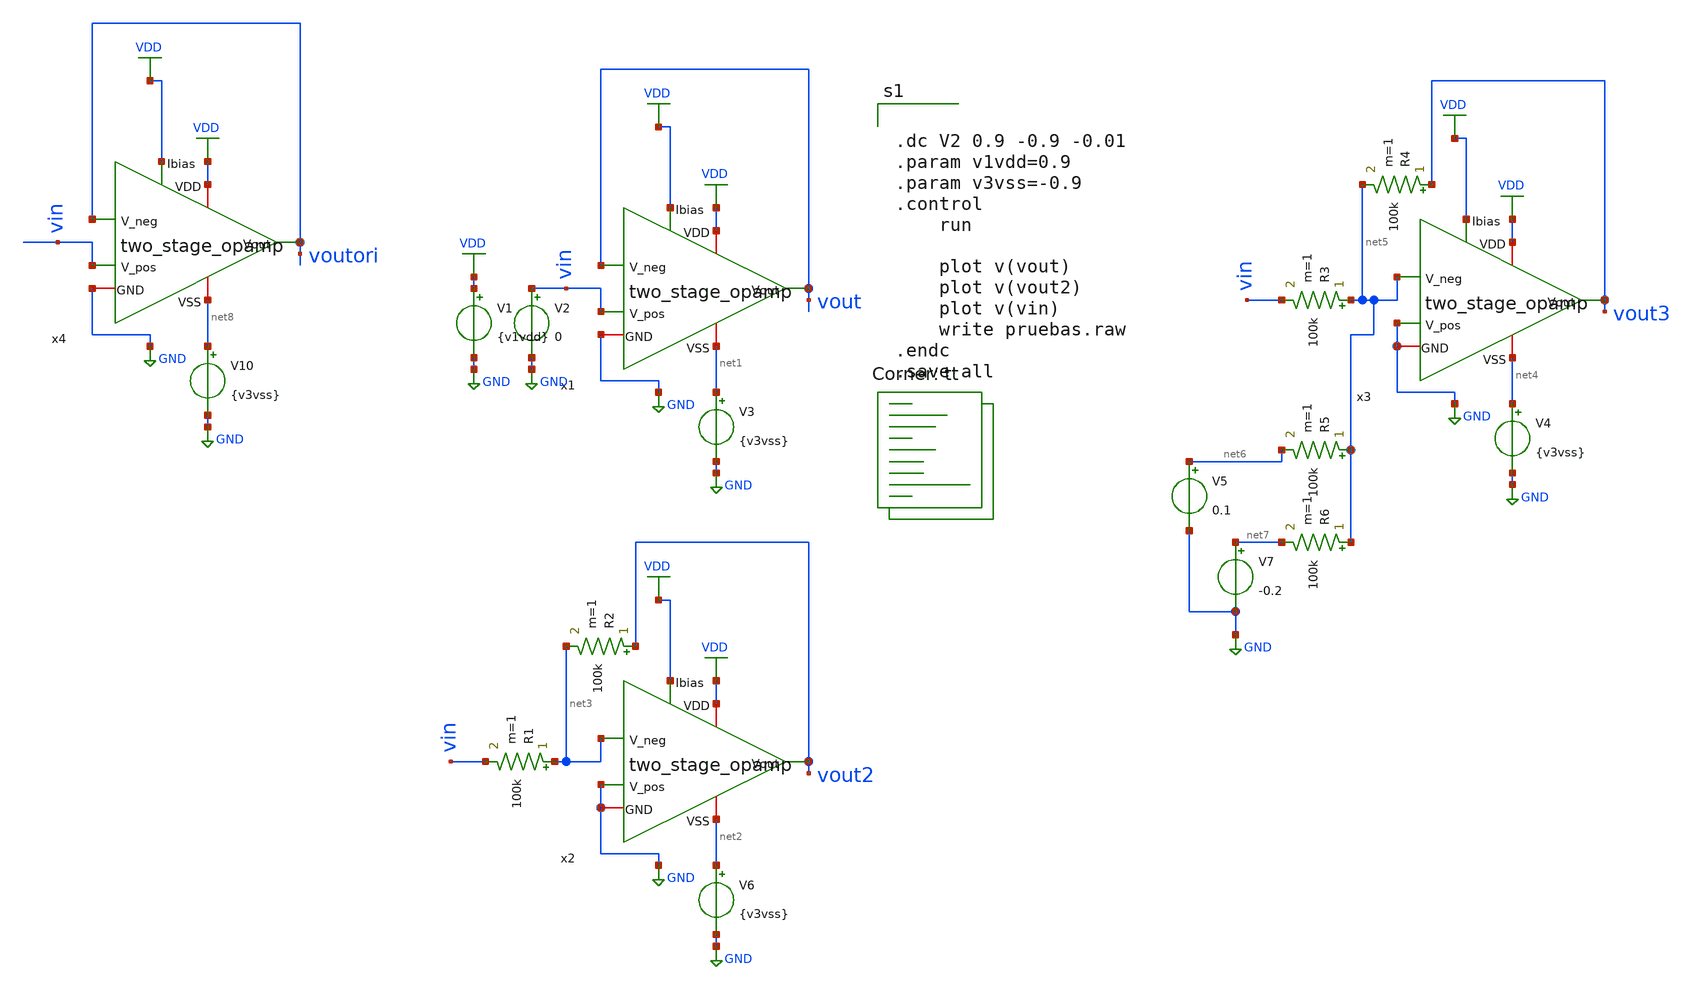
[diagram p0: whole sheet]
** sch_path: two_stage_opamp/pruebas.sch
**.subckt pruebas
x1 VDD vout VDD vout GND vin net1 two_stage_opamp W1=2.13 W2=9 W3=8.7 W4=9 W5=9.8 W6=8.7 L1=0.3965
+ L2=0.3965 L3=0.3965 L4=0.9 L5=1.2 L6=0.8
V1 VDD GND {v1vdd}
V2 vin GND 0
V3 net1 GND {v3vss}
x2 VDD vout2 VDD net3 GND GND net2 two_stage_opamp W1=2.13 W2=9 W3=8.7 W4=9 W5=9.8 W6=8.7 L1=0.3965
+ L2=0.3965 L3=0.3965 L4=0.9 L5=1.2 L6=0.8
V6 net2 GND {v3vss}
R1 net3 vin 100k m=1
R2 vout2 net3 100k m=1
x3 VDD vout3 VDD net5 GND GND net4 two_stage_opamp W1=2.13 W2=9 W3=8.7 W4=9 W5=9.8 W6=8.7 L1=0.3965
+ L2=0.3965 L3=0.3965 L4=0.9 L5=1.2 L6=0.8
V4 net4 GND {v3vss}
R3 net5 vin 100k m=1
R4 vout3 net5 100k m=1
R5 net5 net6 100k m=1
R6 net5 net7 100k m=1
V5 net6 GND 0.1
V7 net7 GND -0.2
x4 VDD voutori VDD voutori GND vin net8 two_stage_opamp W1=15 W2=94 W3=3 W4=4.5 W5=14 W6=10 L1=0.15
+ L2=0.15 L3=0.15 L4=0.15 L5=0.15 L6=0.15
V10 net8 GND {v3vss}
**** begin user architecture code


.dc V2 0.9 -0.9 -0.01
.param v1vdd=0.9
.param v3vss=-0.9
.control
	run

	plot v(vout)
	plot v(vout2)
	plot v(vin)
	write pruebas.raw
.endc
.save all


.lib $::SKYWATER_MODELS/sky130.lib.spice tt
**** end user architecture code
**.ends

* expanding   symbol:
*+  /home/ricardoatt/RATT_repos/Proyectos_xschem/two_stage_opamp/two_stage_opamp.sym # of pins=7
** sym_path: two_stage_opamp/two_stage_opamp.sym
** sch_path: two_stage_opamp/two_stage_opamp.sch
.subckt two_stage_opamp VDD Vout Ibias V_neg GND V_pos VSS  W1=15 W2=94 W3=3 W4=4.5 W5=14 W6=10
+ L1=0.15 L2=0.15 L3=0.15 L4=0.15 L5=0.15 L6=0.15
*.ipin Ibias
*.ipin V_neg
*.ipin V_pos
*.iopin VDD
*.iopin VSS
*.opin Vout
*.iopin GND
XM1 net2 V_neg net4 VSS sky130_fd_pr__nfet_01v8 L=L3 W=W3 nf=1 ad='int((nf+1)/2) * W/nf * 0.29' as='int((nf+2)/2) * W/nf * 0.29'
+ pd='2*int((nf+1)/2) * (W/nf + 0.29)' ps='2*int((nf+2)/2) * (W/nf + 0.29)' nrd='0.29 / W' nrs='0.29 / W'
+ sa=0 sb=0 sd=0 mult=1 m=1
XM3 net2 net2 VDD VDD sky130_fd_pr__pfet_01v8 L=L1 W=W1 nf=1 ad='int((nf+1)/2) * W/nf * 0.29' as='int((nf+2)/2) * W/nf * 0.29'
+ pd='2*int((nf+1)/2) * (W/nf + 0.29)' ps='2*int((nf+2)/2) * (W/nf + 0.29)' nrd='0.29 / W' nrs='0.29 / W'
+ sa=0 sb=0 sd=0 mult=1 m=1
XM2 net3 V_pos net4 VSS sky130_fd_pr__nfet_01v8 L=L3 W=W3 nf=1 ad='int((nf+1)/2) * W/nf * 0.29' as='int((nf+2)/2) * W/nf * 0.29'
+ pd='2*int((nf+1)/2) * (W/nf + 0.29)' ps='2*int((nf+2)/2) * (W/nf + 0.29)' nrd='0.29 / W' nrs='0.29 / W'
+ sa=0 sb=0 sd=0 mult=1 m=1
XM4 net3 net2 VDD VDD sky130_fd_pr__pfet_01v8 L=L1 W=W1 nf=1 ad='int((nf+1)/2) * W/nf * 0.29' as='int((nf+2)/2) * W/nf * 0.29'
+ pd='2*int((nf+1)/2) * (W/nf + 0.29)' ps='2*int((nf+2)/2) * (W/nf + 0.29)' nrd='0.29 / W' nrs='0.29 / W'
+ sa=0 sb=0 sd=0 mult=1 m=1
XM5 net4 net1 VSS VSS sky130_fd_pr__nfet_01v8 L=L4 W=W4 nf=1 ad='int((nf+1)/2) * W/nf * 0.29' as='int((nf+2)/2) * W/nf * 0.29'
+ pd='2*int((nf+1)/2) * (W/nf + 0.29)' ps='2*int((nf+2)/2) * (W/nf + 0.29)' nrd='0.29 / W' nrs='0.29 / W'
+ sa=0 sb=0 sd=0 mult=1 m=1
XM6 Vout net3 VDD VDD sky130_fd_pr__pfet_01v8 L=L2 W=W2 nf=1 ad='int((nf+1)/2) * W/nf * 0.29' as='int((nf+2)/2) * W/nf * 0.29'
+ pd='2*int((nf+1)/2) * (W/nf + 0.29)' ps='2*int((nf+2)/2) * (W/nf + 0.29)' nrd='0.29 / W' nrs='0.29 / W'
+ sa=0 sb=0 sd=0 mult=1 m=1
XM7 Vout net1 VSS VSS sky130_fd_pr__nfet_01v8 L=L5 W=W5 nf=1 ad='int((nf+1)/2) * W/nf * 0.29' as='int((nf+2)/2) * W/nf * 0.29'
+ pd='2*int((nf+1)/2) * (W/nf + 0.29)' ps='2*int((nf+2)/2) * (W/nf + 0.29)' nrd='0.29 / W' nrs='0.29 / W'
+ sa=0 sb=0 sd=0 mult=1 m=1
XM8 net1 net1 VSS VSS sky130_fd_pr__nfet_01v8 L=L4 W=W4 nf=1 ad='int((nf+1)/2) * W/nf * 0.29' as='int((nf+2)/2) * W/nf * 0.29'
+ pd='2*int((nf+1)/2) * (W/nf + 0.29)' ps='2*int((nf+2)/2) * (W/nf + 0.29)' nrd='0.29 / W' nrs='0.29 / W'
+ sa=0 sb=0 sd=0 mult=1 m=1
XM9 net1 net1 Ibias Ibias sky130_fd_pr__pfet_01v8 L=L6 W=W6 nf=1 ad='int((nf+1)/2) * W/nf * 0.29' as='int((nf+2)/2) * W/nf * 0.29'
+ pd='2*int((nf+1)/2) * (W/nf + 0.29)' ps='2*int((nf+2)/2) * (W/nf + 0.29)' nrd='0.29 / W' nrs='0.29 / W'
+ sa=0 sb=0 sd=0 mult=1 m=1
XC1 net3 Vout sky130_fd_pr__cap_mim_m3_1 W=10 L=1 MF=1 m=1
.ends

.GLOBAL VDD
.GLOBAL GND
.end
